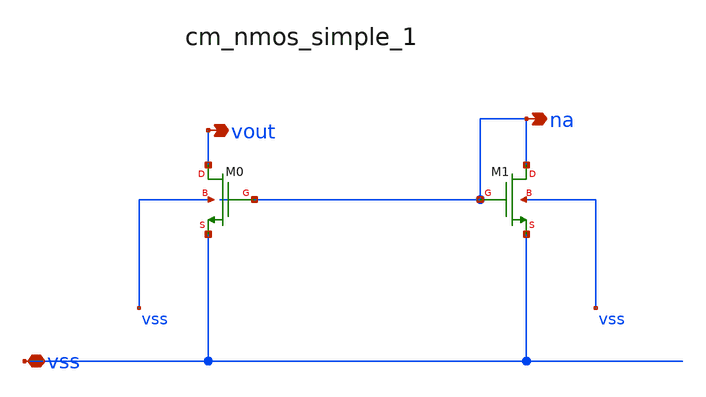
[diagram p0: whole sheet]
** sch_path: analog-db/raw/tsn_003_ptat_4t_xcoupled/hier/blocks/cm_nmos_simple_1.sch
**.subckt cm_nmos_simple_1 vss vout na
*.iopin vss
*.opin vout
*.opin na
XM0 vout na vss vss sg13_lv_nmos w=x_dut_xm0_w l=x_dut_xm0_l ng=1 m=x_dut_xm0_m
XM1 na na vss vss sg13_lv_nmos w=x_dut_xm1_w l=x_dut_xm1_l ng=1 m=x_dut_xm1_m
**.ends
.end
